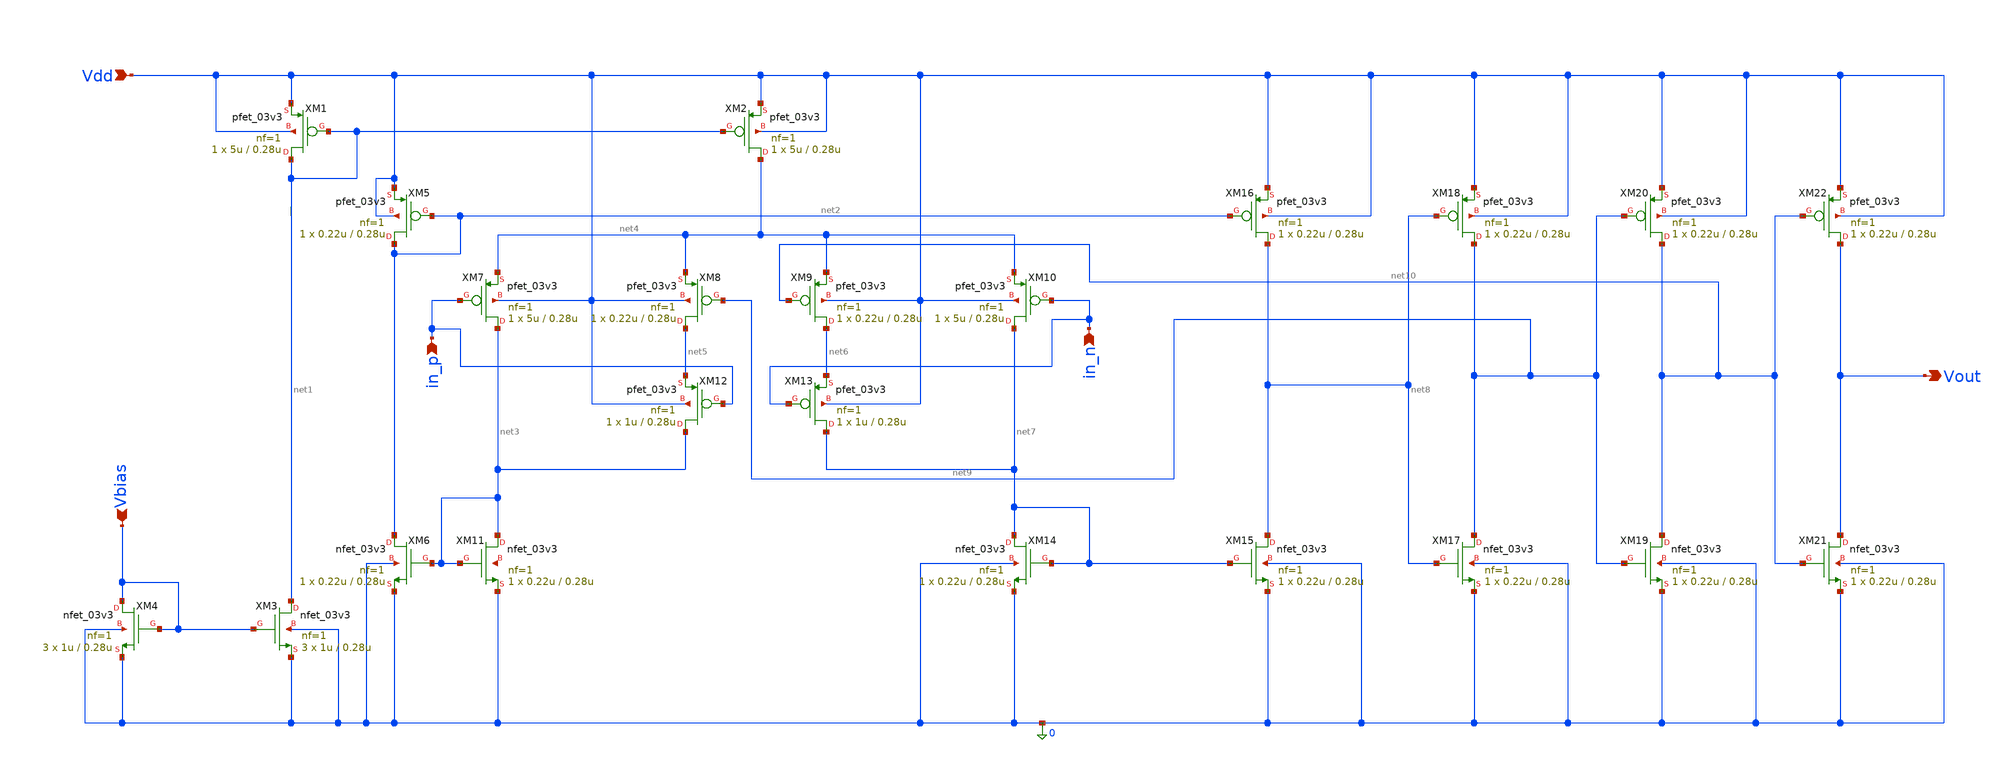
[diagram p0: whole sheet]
** sch_path: blocks/adc/lvds/lvds_rec_v1.sch
**.subckt lvds_rec_v1 Vbias Vdd in_n in_p Vout
*.ipin Vbias
*.ipin Vdd
*.ipin in_n
*.ipin in_p
*.opin Vout
XM1 net1 net1 Vdd Vdd pfet_03v3 L=0.28u W=5u nf=1 ad='int((nf+1)/2) * W/nf * 0.18u' as='int((nf+2)/2) * W/nf * 0.18u'
+ pd='2*int((nf+1)/2) * (W/nf + 0.18u)' ps='2*int((nf+2)/2) * (W/nf + 0.18u)' nrd='0.18u / W' nrs='0.18u / W'
+ sa=0 sb=0 sd=0 m=1
XM2 net4 net1 Vdd Vdd pfet_03v3 L=0.28u W=5u nf=1 ad='int((nf+1)/2) * W/nf * 0.18u' as='int((nf+2)/2) * W/nf * 0.18u'
+ pd='2*int((nf+1)/2) * (W/nf + 0.18u)' ps='2*int((nf+2)/2) * (W/nf + 0.18u)' nrd='0.18u / W' nrs='0.18u / W'
+ sa=0 sb=0 sd=0 m=1
XM3 net1 Vbias 0 0 nfet_03v3 L=0.28u W=1u nf=1 ad='int((nf+1)/2) * W/nf * 0.18u' as='int((nf+2)/2) * W/nf * 0.18u'
+ pd='2*int((nf+1)/2) * (W/nf + 0.18u)' ps='2*int((nf+2)/2) * (W/nf + 0.18u)' nrd='0.18u / W' nrs='0.18u / W'
+ sa=0 sb=0 sd=0 m=3
XM4 Vbias Vbias 0 0 nfet_03v3 L=0.28u W=1u nf=1 ad='int((nf+1)/2) * W/nf * 0.18u' as='int((nf+2)/2) * W/nf * 0.18u'
+ pd='2*int((nf+1)/2) * (W/nf + 0.18u)' ps='2*int((nf+2)/2) * (W/nf + 0.18u)' nrd='0.18u / W' nrs='0.18u / W'
+ sa=0 sb=0 sd=0 m=3
XM5 net2 net2 Vdd Vdd pfet_03v3 L=0.28u W=0.22u nf=1 ad='int((nf+1)/2) * W/nf * 0.18u' as='int((nf+2)/2) * W/nf * 0.18u'
+ pd='2*int((nf+1)/2) * (W/nf + 0.18u)' ps='2*int((nf+2)/2) * (W/nf + 0.18u)' nrd='0.18u / W' nrs='0.18u / W'
+ sa=0 sb=0 sd=0 m=1
XM6 net2 net3 0 0 nfet_03v3 L=0.28u W=0.22u nf=1 ad='int((nf+1)/2) * W/nf * 0.18u' as='int((nf+2)/2) * W/nf * 0.18u'
+ pd='2*int((nf+1)/2) * (W/nf + 0.18u)' ps='2*int((nf+2)/2) * (W/nf + 0.18u)' nrd='0.18u / W' nrs='0.18u / W'
+ sa=0 sb=0 sd=0 m=1
XM7 net3 in_p net4 Vdd pfet_03v3 L=0.28u W=5u nf=1 ad='int((nf+1)/2) * W/nf * 0.18u' as='int((nf+2)/2) * W/nf * 0.18u'
+ pd='2*int((nf+1)/2) * (W/nf + 0.18u)' ps='2*int((nf+2)/2) * (W/nf + 0.18u)' nrd='0.18u / W' nrs='0.18u / W'
+ sa=0 sb=0 sd=0 m=1
XM8 net5 net9 net4 Vdd pfet_03v3 L=0.28u W=0.22u nf=1 ad='int((nf+1)/2) * W/nf * 0.18u' as='int((nf+2)/2) * W/nf * 0.18u'
+ pd='2*int((nf+1)/2) * (W/nf + 0.18u)' ps='2*int((nf+2)/2) * (W/nf + 0.18u)' nrd='0.18u / W' nrs='0.18u / W'
+ sa=0 sb=0 sd=0 m=1
XM9 net6 net10 net4 Vdd pfet_03v3 L=0.28u W=0.22u nf=1 ad='int((nf+1)/2) * W/nf * 0.18u' as='int((nf+2)/2) * W/nf * 0.18u'
+ pd='2*int((nf+1)/2) * (W/nf + 0.18u)' ps='2*int((nf+2)/2) * (W/nf + 0.18u)' nrd='0.18u / W' nrs='0.18u / W'
+ sa=0 sb=0 sd=0 m=1
XM10 net7 in_n net4 Vdd pfet_03v3 L=0.28u W=5u nf=1 ad='int((nf+1)/2) * W/nf * 0.18u' as='int((nf+2)/2) * W/nf * 0.18u'
+ pd='2*int((nf+1)/2) * (W/nf + 0.18u)' ps='2*int((nf+2)/2) * (W/nf + 0.18u)' nrd='0.18u / W' nrs='0.18u / W'
+ sa=0 sb=0 sd=0 m=1
XM11 net3 net3 0 net11 nfet_03v3 L=0.28u W=0.22u nf=1 ad='int((nf+1)/2) * W/nf * 0.18u' as='int((nf+2)/2) * W/nf * 0.18u'
+ pd='2*int((nf+1)/2) * (W/nf + 0.18u)' ps='2*int((nf+2)/2) * (W/nf + 0.18u)' nrd='0.18u / W' nrs='0.18u / W'
+ sa=0 sb=0 sd=0 m=1
XM12 net3 in_p net5 Vdd pfet_03v3 L=0.28u W=1u nf=1 ad='int((nf+1)/2) * W/nf * 0.18u' as='int((nf+2)/2) * W/nf * 0.18u'
+ pd='2*int((nf+1)/2) * (W/nf + 0.18u)' ps='2*int((nf+2)/2) * (W/nf + 0.18u)' nrd='0.18u / W' nrs='0.18u / W'
+ sa=0 sb=0 sd=0 m=1
XM13 net7 in_n net6 Vdd pfet_03v3 L=0.28u W=1u nf=1 ad='int((nf+1)/2) * W/nf * 0.18u' as='int((nf+2)/2) * W/nf * 0.18u'
+ pd='2*int((nf+1)/2) * (W/nf + 0.18u)' ps='2*int((nf+2)/2) * (W/nf + 0.18u)' nrd='0.18u / W' nrs='0.18u / W'
+ sa=0 sb=0 sd=0 m=1
XM14 net7 net7 0 0 nfet_03v3 L=0.28u W=0.22u nf=1 ad='int((nf+1)/2) * W/nf * 0.18u' as='int((nf+2)/2) * W/nf * 0.18u'
+ pd='2*int((nf+1)/2) * (W/nf + 0.18u)' ps='2*int((nf+2)/2) * (W/nf + 0.18u)' nrd='0.18u / W' nrs='0.18u / W'
+ sa=0 sb=0 sd=0 m=1
XM15 net8 net7 0 0 nfet_03v3 L=0.28u W=0.22u nf=1 ad='int((nf+1)/2) * W/nf * 0.18u' as='int((nf+2)/2) * W/nf * 0.18u'
+ pd='2*int((nf+1)/2) * (W/nf + 0.18u)' ps='2*int((nf+2)/2) * (W/nf + 0.18u)' nrd='0.18u / W' nrs='0.18u / W'
+ sa=0 sb=0 sd=0 m=1
XM16 net8 net2 Vdd Vdd pfet_03v3 L=0.28u W=0.22u nf=1 ad='int((nf+1)/2) * W/nf * 0.18u' as='int((nf+2)/2) * W/nf * 0.18u'
+ pd='2*int((nf+1)/2) * (W/nf + 0.18u)' ps='2*int((nf+2)/2) * (W/nf + 0.18u)' nrd='0.18u / W' nrs='0.18u / W'
+ sa=0 sb=0 sd=0 m=1
XM17 net9 net8 0 0 nfet_03v3 L=0.28u W=0.22u nf=1 ad='int((nf+1)/2) * W/nf * 0.18u' as='int((nf+2)/2) * W/nf * 0.18u'
+ pd='2*int((nf+1)/2) * (W/nf + 0.18u)' ps='2*int((nf+2)/2) * (W/nf + 0.18u)' nrd='0.18u / W' nrs='0.18u / W'
+ sa=0 sb=0 sd=0 m=1
XM18 net9 net8 Vdd Vdd pfet_03v3 L=0.28u W=0.22u nf=1 ad='int((nf+1)/2) * W/nf * 0.18u' as='int((nf+2)/2) * W/nf * 0.18u'
+ pd='2*int((nf+1)/2) * (W/nf + 0.18u)' ps='2*int((nf+2)/2) * (W/nf + 0.18u)' nrd='0.18u / W' nrs='0.18u / W'
+ sa=0 sb=0 sd=0 m=1
XM19 net10 net9 0 0 nfet_03v3 L=0.28u W=0.22u nf=1 ad='int((nf+1)/2) * W/nf * 0.18u' as='int((nf+2)/2) * W/nf * 0.18u'
+ pd='2*int((nf+1)/2) * (W/nf + 0.18u)' ps='2*int((nf+2)/2) * (W/nf + 0.18u)' nrd='0.18u / W' nrs='0.18u / W'
+ sa=0 sb=0 sd=0 m=1
XM20 net10 net9 Vdd Vdd pfet_03v3 L=0.28u W=0.22u nf=1 ad='int((nf+1)/2) * W/nf * 0.18u' as='int((nf+2)/2) * W/nf * 0.18u'
+ pd='2*int((nf+1)/2) * (W/nf + 0.18u)' ps='2*int((nf+2)/2) * (W/nf + 0.18u)' nrd='0.18u / W' nrs='0.18u / W'
+ sa=0 sb=0 sd=0 m=1
XM21 Vout net10 0 0 nfet_03v3 L=0.28u W=0.22u nf=1 ad='int((nf+1)/2) * W/nf * 0.18u' as='int((nf+2)/2) * W/nf * 0.18u'
+ pd='2*int((nf+1)/2) * (W/nf + 0.18u)' ps='2*int((nf+2)/2) * (W/nf + 0.18u)' nrd='0.18u / W' nrs='0.18u / W'
+ sa=0 sb=0 sd=0 m=1
XM22 Vout net10 Vdd Vdd pfet_03v3 L=0.28u W=0.22u nf=1 ad='int((nf+1)/2) * W/nf * 0.18u' as='int((nf+2)/2) * W/nf * 0.18u'
+ pd='2*int((nf+1)/2) * (W/nf + 0.18u)' ps='2*int((nf+2)/2) * (W/nf + 0.18u)' nrd='0.18u / W' nrs='0.18u / W'
+ sa=0 sb=0 sd=0 m=1
**.ends
.end
